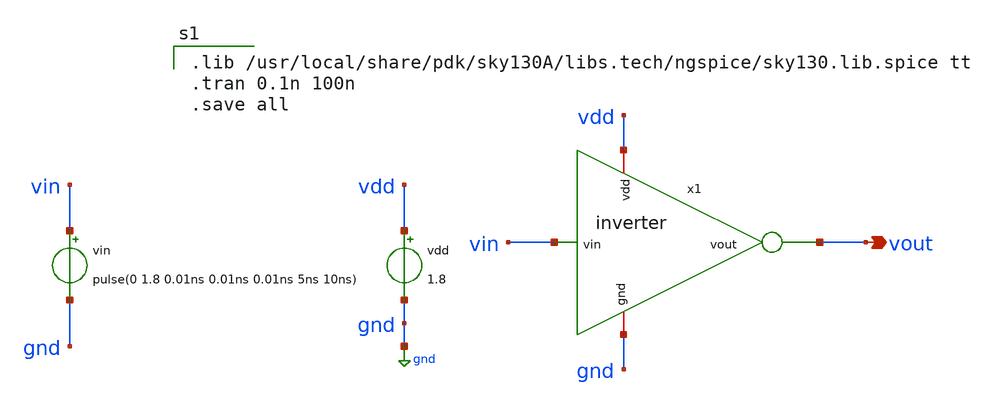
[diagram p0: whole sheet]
** sch_path: LogicGates/inverter_tb.sch
**.subckt inverter_tb vout
*.opin vout
x1 vdd vout vin gnd inverter
vin vin gnd pulse(0 1.8 0.01ns 0.01ns 0.01ns 5ns 10ns)
vdd vdd gnd 1.8
**** begin user architecture code

.lib /usr/local/share/pdk/sky130A/libs.tech/ngspice/sky130.lib.spice tt
.tran 0.1n 100n
.save all

**** end user architecture code
**.ends

* expanding   symbol:  inverter.sym # of pins=4
** sym_path: LogicGates/inverter.sym
** sch_path: LogicGates/inverter.sch
.subckt inverter vdd vout vin gnd
*.ipin vin
*.opin vout
*.iopin vdd
*.iopin gnd
XM1 vout vin net2 net2 sky130_fd_pr__nfet_01v8 L=0.15 W=1 nf=1 ad='int((nf+1)/2) * W/nf * 0.29' as='int((nf+2)/2) * W/nf * 0.29'
+ pd='2*int((nf+1)/2) * (W/nf + 0.29)' ps='2*int((nf+2)/2) * (W/nf + 0.29)' nrd='0.29 / W' nrs='0.29 / W'
+ sa=0 sb=0 sd=0 mult=1 m=1
XM2 vout vin net1 net1 sky130_fd_pr__pfet_01v8 L=0.15 W=2 nf=1 ad='int((nf+1)/2) * W/nf * 0.29' as='int((nf+2)/2) * W/nf * 0.29'
+ pd='2*int((nf+1)/2) * (W/nf + 0.29)' ps='2*int((nf+2)/2) * (W/nf + 0.29)' nrd='0.29 / W' nrs='0.29 / W'
+ sa=0 sb=0 sd=0 mult=1 m=1
.ends

.GLOBAL gnd
.end
